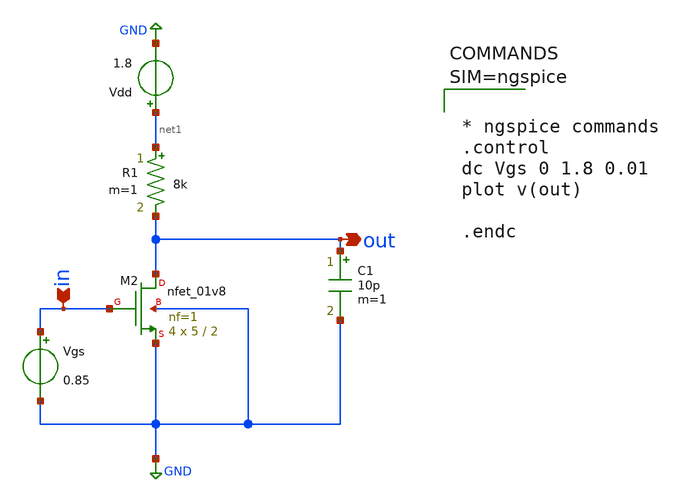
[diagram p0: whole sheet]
** sch_path: xschem/mos.sch
**.subckt mos in out
*.ipin in
*.opin out
XM2 out in GND GND sky130_fd_pr__nfet_01v8 L=2 W=5 nf=1 ad='int((1 + 1)/2) * 5 / 1 * 0.29' as='int((1 + 2)/2) * 5 / 1 * 0.29'
+ pd='2*int((1 + 1)/2) * (5 / 1 + 0.29)' ps='2*int((1 + 2)/2) * (5 / 1 + 0.29)' nrd='0.29 / 5 ' nrs='0.29 / 5 '
+ sa=0 sb=0 sd=0 mult=4 m=4
Vgs in GND 0.85
C1 out GND 10p m=1
R1 net1 out 8k m=1
Vdd net1 GND 1.8
**** begin user architecture code

** opencircuitdesign pdks install
.lib $::SKYWATER_MODELS/sky130.lib.spice tt




* ngspice commands
.control
dc Vgs 0 1.8 0.01
plot v(out)

.endc



**** end user architecture code
**.ends
.GLOBAL GND
.end
